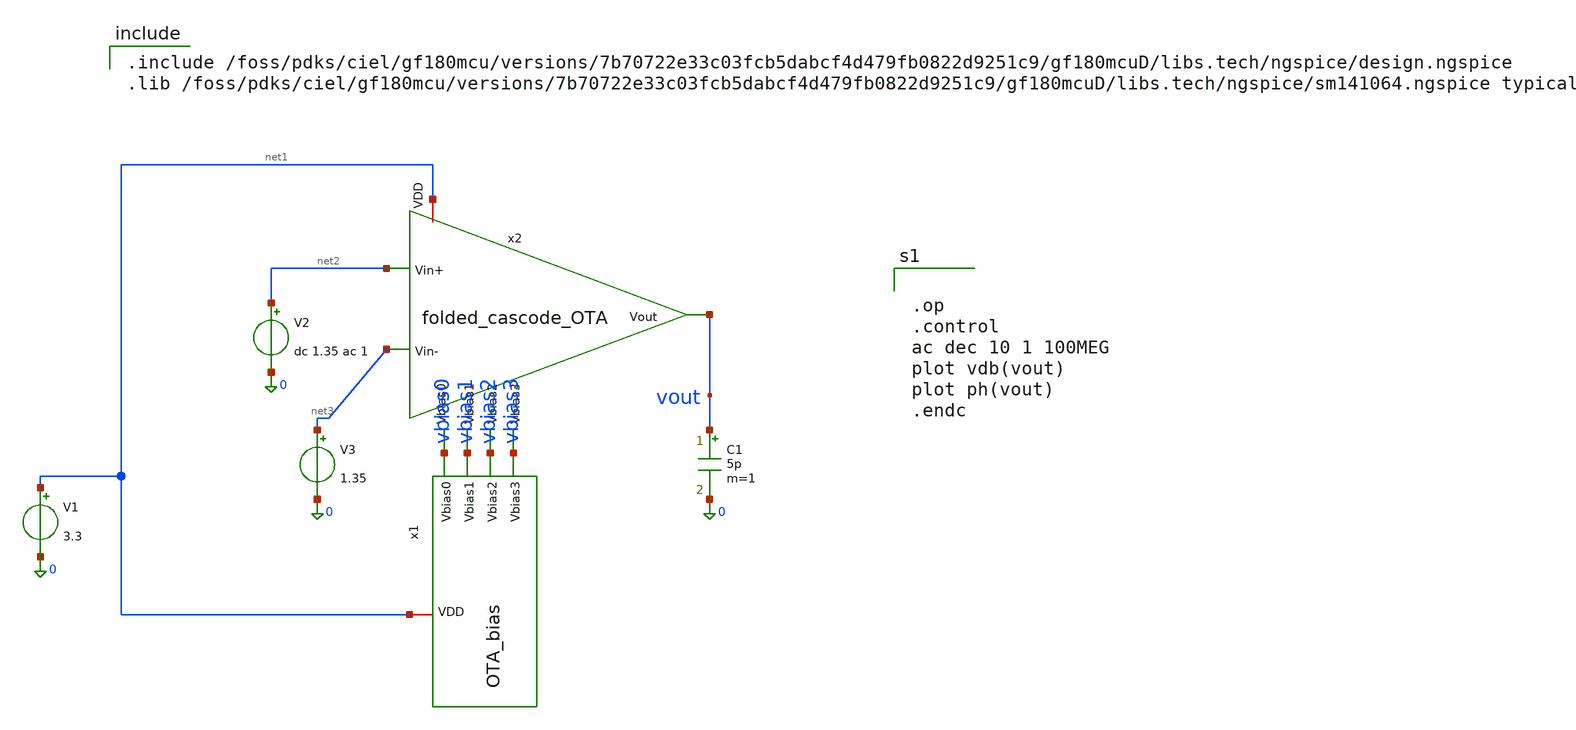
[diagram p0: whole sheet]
** sch_path: analog/Test_ota_bias.sch
**.subckt Test_ota_bias
x1 net1 vbias0 vbias2 vbias3 vbias1 OTA_bias
x2 net1 vbias0 net2 net3 vbias3 vbias1 vout vbias2 folded_cascode_OTA
V1 net1 0 3.3
V2 net2 0 dc 1.35 ac 1
V3 net3 0 1.35
C1 vout 0 5p m=1
**** begin user architecture code

.include /foss/pdks/ciel/gf180mcu/versions/7b70722e33c03fcb5dabcf4d479fb0822d9251c9/gf180mcuD/libs.tech/ngspice/design.ngspice
.lib /foss/pdks/ciel/gf180mcu/versions/7b70722e33c03fcb5dabcf4d479fb0822d9251c9/gf180mcuD/libs.tech/ngspice/sm141064.ngspice typical



.op
.control
ac dec 10 1 100MEG
plot vdb(vout)
plot ph(vout)
.endc


**** end user architecture code
**.ends

* expanding   symbol:  AURA/OTA_bias.sym # of pins=5
** sym_path: analog/OTA_bias.sym
** sch_path: analog/OTA_bias.sch
.subckt OTA_bias VDD Vbias0 Vbias2 Vbias3 Vbias1
*.iopin VDD
*.opin Vbias2
*.opin Vbias1
*.opin Vbias0
*.opin Vbias3
**** begin user architecture code

.include /foss/pdks/ciel/gf180mcu/versions/7b70722e33c03fcb5dabcf4d479fb0822d9251c9/gf180mcuD/libs.tech/ngspice/design.ngspice
.lib /foss/pdks/ciel/gf180mcu/versions/7b70722e33c03fcb5dabcf4d479fb0822d9251c9/gf180mcuD/libs.tech/ngspice/sm141064.ngspice typical

**** end user architecture code
XM1 Vbias1 0 Vbias2 VDD pfet_03v3 L=1u W=2u nf=1 ad='int((nf+1)/2) * W/nf * 0.18u' as='int((nf+2)/2) * W/nf * 0.18u'
+ pd='2*int((nf+1)/2) * (W/nf + 0.18u)' ps='2*int((nf+2)/2) * (W/nf + 0.18u)' nrd='0.18u / W' nrs='0.18u / W'
+ sa=0 sb=0 sd=0 m=1
XM4 Vbias1 Vbias2 net1 0 nfet_03v3 L=1u W=2u nf=1 ad='int((nf+1)/2) * W/nf * 0.18u' as='int((nf+2)/2) * W/nf * 0.18u'
+ pd='2*int((nf+1)/2) * (W/nf + 0.18u)' ps='2*int((nf+2)/2) * (W/nf + 0.18u)' nrd='0.18u / W' nrs='0.18u / W'
+ sa=0 sb=0 sd=0 m=1
XM5 net1 Vbias1 0 0 nfet_03v3 L=1u W=2u nf=1 ad='int((nf+1)/2) * W/nf * 0.18u' as='int((nf+2)/2) * W/nf * 0.18u'
+ pd='2*int((nf+1)/2) * (W/nf + 0.18u)' ps='2*int((nf+2)/2) * (W/nf + 0.18u)' nrd='0.18u / W' nrs='0.18u / W'
+ sa=0 sb=0 sd=0 m=1
XM9 net2 Vbias3 Vbias0 VDD pfet_03v3 L=1u W=2u nf=1 ad='int((nf+1)/2) * W/nf * 0.18u' as='int((nf+2)/2) * W/nf * 0.18u'
+ pd='2*int((nf+1)/2) * (W/nf + 0.18u)' ps='2*int((nf+2)/2) * (W/nf + 0.18u)' nrd='0.18u / W' nrs='0.18u / W'
+ sa=0 sb=0 sd=0 m=1
XM10 VDD Vbias0 net2 VDD pfet_03v3 L=1u W=2u nf=1 ad='int((nf+1)/2) * W/nf * 0.18u' as='int((nf+2)/2) * W/nf * 0.18u'
+ pd='2*int((nf+1)/2) * (W/nf + 0.18u)' ps='2*int((nf+2)/2) * (W/nf + 0.18u)' nrd='0.18u / W' nrs='0.18u / W'
+ sa=0 sb=0 sd=0 m=1
XM6 Vbias3 VDD Vbias0 0 nfet_03v3 L=1u W=2u nf=1 ad='int((nf+1)/2) * W/nf * 0.18u' as='int((nf+2)/2) * W/nf * 0.18u'
+ pd='2*int((nf+1)/2) * (W/nf + 0.18u)' ps='2*int((nf+2)/2) * (W/nf + 0.18u)' nrd='0.18u / W' nrs='0.18u / W'
+ sa=0 sb=0 sd=0 m=1
I0 VDD Vbias2 200n
I1 Vbias3 0 200n
.ends


* expanding   symbol:  AURA/folded_cascode_OTA.sym # of pins=8
** sym_path: analog/folded_cascode_OTA.sym
** sch_path: analog/folded_cascode_OTA.sch
.subckt folded_cascode_OTA VDD Vbias0 Vin+ Vin- Vbias3 Vbias1 Vout Vbias2
*.iopin VDD
*.ipin Vbias0
*.ipin Vin+
*.ipin Vin-
*.ipin Vbias1
*.opin Vout
*.ipin Vbias3
*.ipin Vbias2
XM1 net1 Vbias0 VDD VDD pfet_03v3 L=1u W=2u nf=2 ad='int((nf+1)/2) * W/nf * 0.18u' as='int((nf+2)/2) * W/nf * 0.18u'
+ pd='2*int((nf+1)/2) * (W/nf + 0.18u)' ps='2*int((nf+2)/2) * (W/nf + 0.18u)' nrd='0.18u / W' nrs='0.18u / W'
+ sa=0 sb=0 sd=0 m=1
XM2 net6 Vin+ net1 net1 pfet_03v3 L=1u W=2u nf=9 ad='int((nf+1)/2) * W/nf * 0.18u' as='int((nf+2)/2) * W/nf * 0.18u'
+ pd='2*int((nf+1)/2) * (W/nf + 0.18u)' ps='2*int((nf+2)/2) * (W/nf + 0.18u)' nrd='0.18u / W' nrs='0.18u / W'
+ sa=0 sb=0 sd=0 m=1
XM3 net7 Vin- net1 net1 pfet_03v3 L=1u W=2u nf=9 ad='int((nf+1)/2) * W/nf * 0.18u' as='int((nf+2)/2) * W/nf * 0.18u'
+ pd='2*int((nf+1)/2) * (W/nf + 0.18u)' ps='2*int((nf+2)/2) * (W/nf + 0.18u)' nrd='0.18u / W' nrs='0.18u / W'
+ sa=0 sb=0 sd=0 m=1
XM4 net2 Vin+ net1 net1 pfet_03v3 L=1u W=2u nf=1 ad='int((nf+1)/2) * W/nf * 0.18u' as='int((nf+2)/2) * W/nf * 0.18u'
+ pd='2*int((nf+1)/2) * (W/nf + 0.18u)' ps='2*int((nf+2)/2) * (W/nf + 0.18u)' nrd='0.18u / W' nrs='0.18u / W'
+ sa=0 sb=0 sd=0 m=1
XM5 net3 Vin- net1 net1 pfet_03v3 L=1u W=2u nf=1 ad='int((nf+1)/2) * W/nf * 0.18u' as='int((nf+2)/2) * W/nf * 0.18u'
+ pd='2*int((nf+1)/2) * (W/nf + 0.18u)' ps='2*int((nf+2)/2) * (W/nf + 0.18u)' nrd='0.18u / W' nrs='0.18u / W'
+ sa=0 sb=0 sd=0 m=1
XM6 net2 Vbias2 net5 0 nfet_03v3 L=1u W=2u nf=1 ad='int((nf+1)/2) * W/nf * 0.18u' as='int((nf+2)/2) * W/nf * 0.18u'
+ pd='2*int((nf+1)/2) * (W/nf + 0.18u)' ps='2*int((nf+2)/2) * (W/nf + 0.18u)' nrd='0.18u / W' nrs='0.18u / W'
+ sa=0 sb=0 sd=0 m=1
XM7 net3 Vbias2 net4 0 nfet_03v3 L=1u W=2u nf=1 ad='int((nf+1)/2) * W/nf * 0.18u' as='int((nf+2)/2) * W/nf * 0.18u'
+ pd='2*int((nf+1)/2) * (W/nf + 0.18u)' ps='2*int((nf+2)/2) * (W/nf + 0.18u)' nrd='0.18u / W' nrs='0.18u / W'
+ sa=0 sb=0 sd=0 m=1
XM8 net5 net2 0 0 nfet_03v3 L=2u W=2u nf=1 ad='int((nf+1)/2) * W/nf * 0.18u' as='int((nf+2)/2) * W/nf * 0.18u'
+ pd='2*int((nf+1)/2) * (W/nf + 0.18u)' ps='2*int((nf+2)/2) * (W/nf + 0.18u)' nrd='0.18u / W' nrs='0.18u / W'
+ sa=0 sb=0 sd=0 m=1
XM9 net6 net3 0 0 nfet_03v3 L=2u W=2u nf=1 ad='int((nf+1)/2) * W/nf * 0.18u' as='int((nf+2)/2) * W/nf * 0.18u'
+ pd='2*int((nf+1)/2) * (W/nf + 0.18u)' ps='2*int((nf+2)/2) * (W/nf + 0.18u)' nrd='0.18u / W' nrs='0.18u / W'
+ sa=0 sb=0 sd=0 m=1
XM10 net4 net3 0 0 nfet_03v3 L=2u W=2u nf=1 ad='int((nf+1)/2) * W/nf * 0.18u' as='int((nf+2)/2) * W/nf * 0.18u'
+ pd='2*int((nf+1)/2) * (W/nf + 0.18u)' ps='2*int((nf+2)/2) * (W/nf + 0.18u)' nrd='0.18u / W' nrs='0.18u / W'
+ sa=0 sb=0 sd=0 m=1
XM11 net7 net2 0 0 nfet_03v3 L=2u W=2u nf=1 ad='int((nf+1)/2) * W/nf * 0.18u' as='int((nf+2)/2) * W/nf * 0.18u'
+ pd='2*int((nf+1)/2) * (W/nf + 0.18u)' ps='2*int((nf+2)/2) * (W/nf + 0.18u)' nrd='0.18u / W' nrs='0.18u / W'
+ sa=0 sb=0 sd=0 m=1
XM12 net9 net10 VDD VDD pfet_03v3 L=1u W=2u nf=1 ad='int((nf+1)/2) * W/nf * 0.18u' as='int((nf+2)/2) * W/nf * 0.18u'
+ pd='2*int((nf+1)/2) * (W/nf + 0.18u)' ps='2*int((nf+2)/2) * (W/nf + 0.18u)' nrd='0.18u / W' nrs='0.18u / W'
+ sa=0 sb=0 sd=0 m=1
XM13 net8 net10 VDD VDD pfet_03v3 L=1u W=2u nf=1 ad='int((nf+1)/2) * W/nf * 0.18u' as='int((nf+2)/2) * W/nf * 0.18u'
+ pd='2*int((nf+1)/2) * (W/nf + 0.18u)' ps='2*int((nf+2)/2) * (W/nf + 0.18u)' nrd='0.18u / W' nrs='0.18u / W'
+ sa=0 sb=0 sd=0 m=1
XM14 Vout Vbias3 net9 net9 pfet_03v3 L=1u W=2u nf=1 ad='int((nf+1)/2) * W/nf * 0.18u' as='int((nf+2)/2) * W/nf * 0.18u'
+ pd='2*int((nf+1)/2) * (W/nf + 0.18u)' ps='2*int((nf+2)/2) * (W/nf + 0.18u)' nrd='0.18u / W' nrs='0.18u / W'
+ sa=0 sb=0 sd=0 m=1
XM15 net10 Vbias3 net8 net8 pfet_03v3 L=1u W=2u nf=1 ad='int((nf+1)/2) * W/nf * 0.18u' as='int((nf+2)/2) * W/nf * 0.18u'
+ pd='2*int((nf+1)/2) * (W/nf + 0.18u)' ps='2*int((nf+2)/2) * (W/nf + 0.18u)' nrd='0.18u / W' nrs='0.18u / W'
+ sa=0 sb=0 sd=0 m=1
XM16 Vout Vbias1 net7 0 nfet_03v3 L=1u W=2u nf=1 ad='int((nf+1)/2) * W/nf * 0.18u' as='int((nf+2)/2) * W/nf * 0.18u'
+ pd='2*int((nf+1)/2) * (W/nf + 0.18u)' ps='2*int((nf+2)/2) * (W/nf + 0.18u)' nrd='0.18u / W' nrs='0.18u / W'
+ sa=0 sb=0 sd=0 m=1
XM17 net10 Vbias1 net6 0 nfet_03v3 L=1u W=2u nf=1 ad='int((nf+1)/2) * W/nf * 0.18u' as='int((nf+2)/2) * W/nf * 0.18u'
+ pd='2*int((nf+1)/2) * (W/nf + 0.18u)' ps='2*int((nf+2)/2) * (W/nf + 0.18u)' nrd='0.18u / W' nrs='0.18u / W'
+ sa=0 sb=0 sd=0 m=1
.ends

.end
